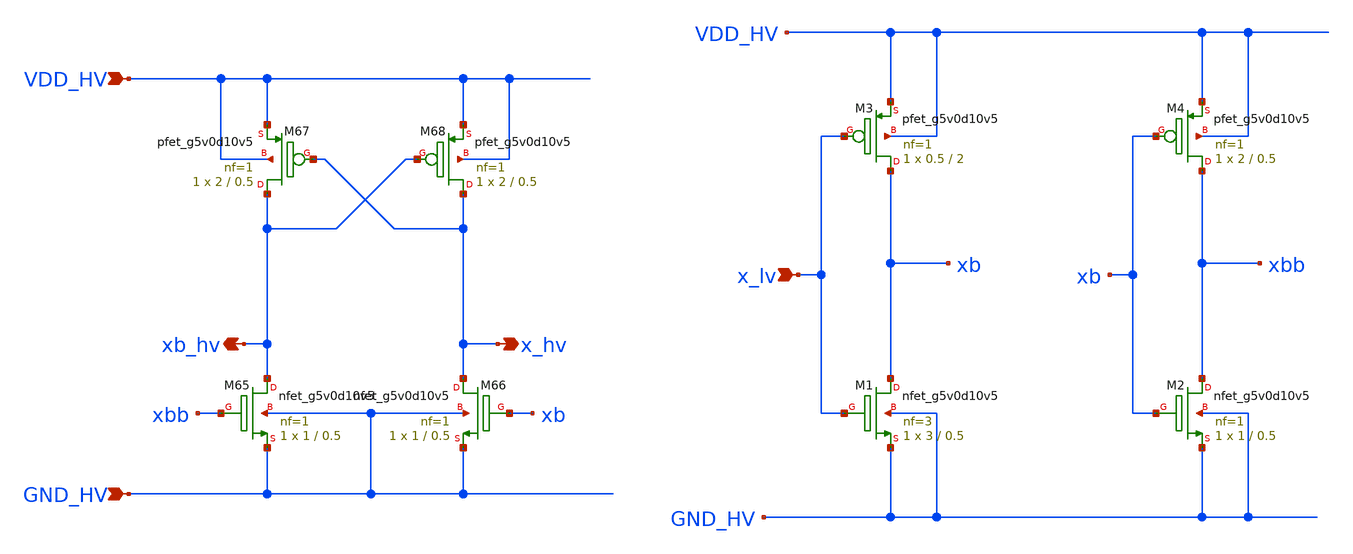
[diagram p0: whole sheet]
** sch_path: xschem/level_shifter_up.sch
**.subckt level_shifter_up VDD_HV GND_HV x_lv x_hv xb_hv
*.ipin VDD_HV
*.ipin GND_HV
*.ipin x_lv
*.opin x_hv
*.opin xb_hv
XM65 xb_hv xbb GND_HV GND_HV sky130_fd_pr__nfet_g5v0d10v5 L=0.5 W=1 nf=1 ad='int((nf+1)/2) * W/nf * 0.29'
+ as='int((nf+2)/2) * W/nf * 0.29' pd='2*int((nf+1)/2) * (W/nf + 0.29)' ps='2*int((nf+2)/2) * (W/nf + 0.29)'
+ nrd='0.29 / W' nrs='0.29 / W' sa=0 sb=0 sd=0 mult=1 m=1
XM66 x_hv xb GND_HV GND_HV sky130_fd_pr__nfet_g5v0d10v5 L=0.5 W=1 nf=1 ad='int((nf+1)/2) * W/nf * 0.29'
+ as='int((nf+2)/2) * W/nf * 0.29' pd='2*int((nf+1)/2) * (W/nf + 0.29)' ps='2*int((nf+2)/2) * (W/nf + 0.29)'
+ nrd='0.29 / W' nrs='0.29 / W' sa=0 sb=0 sd=0 mult=1 m=1
XM67 xb_hv x_hv VDD_HV VDD_HV sky130_fd_pr__pfet_g5v0d10v5 L=0.5 W=2 nf=1 ad='int((nf+1)/2) * W/nf * 0.29'
+ as='int((nf+2)/2) * W/nf * 0.29' pd='2*int((nf+1)/2) * (W/nf + 0.29)' ps='2*int((nf+2)/2) * (W/nf + 0.29)'
+ nrd='0.29 / W' nrs='0.29 / W' sa=0 sb=0 sd=0 mult=1 m=1
XM68 x_hv xb_hv VDD_HV VDD_HV sky130_fd_pr__pfet_g5v0d10v5 L=0.5 W=2 nf=1 ad='int((nf+1)/2) * W/nf * 0.29'
+ as='int((nf+2)/2) * W/nf * 0.29' pd='2*int((nf+1)/2) * (W/nf + 0.29)' ps='2*int((nf+2)/2) * (W/nf + 0.29)'
+ nrd='0.29 / W' nrs='0.29 / W' sa=0 sb=0 sd=0 mult=1 m=1
XM1 xb x_lv GND_HV GND_HV sky130_fd_pr__nfet_g5v0d10v5 L=0.5 W=3 nf=3 ad='int((nf+1)/2) * W/nf * 0.29'
+ as='int((nf+2)/2) * W/nf * 0.29' pd='2*int((nf+1)/2) * (W/nf + 0.29)' ps='2*int((nf+2)/2) * (W/nf + 0.29)'
+ nrd='0.29 / W' nrs='0.29 / W' sa=0 sb=0 sd=0 mult=1 m=1
XM2 xbb xb GND_HV GND_HV sky130_fd_pr__nfet_g5v0d10v5 L=0.5 W=1 nf=1 ad='int((nf+1)/2) * W/nf * 0.29'
+ as='int((nf+2)/2) * W/nf * 0.29' pd='2*int((nf+1)/2) * (W/nf + 0.29)' ps='2*int((nf+2)/2) * (W/nf + 0.29)'
+ nrd='0.29 / W' nrs='0.29 / W' sa=0 sb=0 sd=0 mult=1 m=1
XM3 xb x_lv VDD_HV VDD_HV sky130_fd_pr__pfet_g5v0d10v5 L=2 W=0.5 nf=1 ad='int((nf+1)/2) * W/nf * 0.29'
+ as='int((nf+2)/2) * W/nf * 0.29' pd='2*int((nf+1)/2) * (W/nf + 0.29)' ps='2*int((nf+2)/2) * (W/nf + 0.29)'
+ nrd='0.29 / W' nrs='0.29 / W' sa=0 sb=0 sd=0 mult=1 m=1
XM4 xbb xb VDD_HV VDD_HV sky130_fd_pr__pfet_g5v0d10v5 L=0.5 W=2 nf=1 ad='int((nf+1)/2) * W/nf * 0.29'
+ as='int((nf+2)/2) * W/nf * 0.29' pd='2*int((nf+1)/2) * (W/nf + 0.29)' ps='2*int((nf+2)/2) * (W/nf + 0.29)'
+ nrd='0.29 / W' nrs='0.29 / W' sa=0 sb=0 sd=0 mult=1 m=1
**.ends
.end
